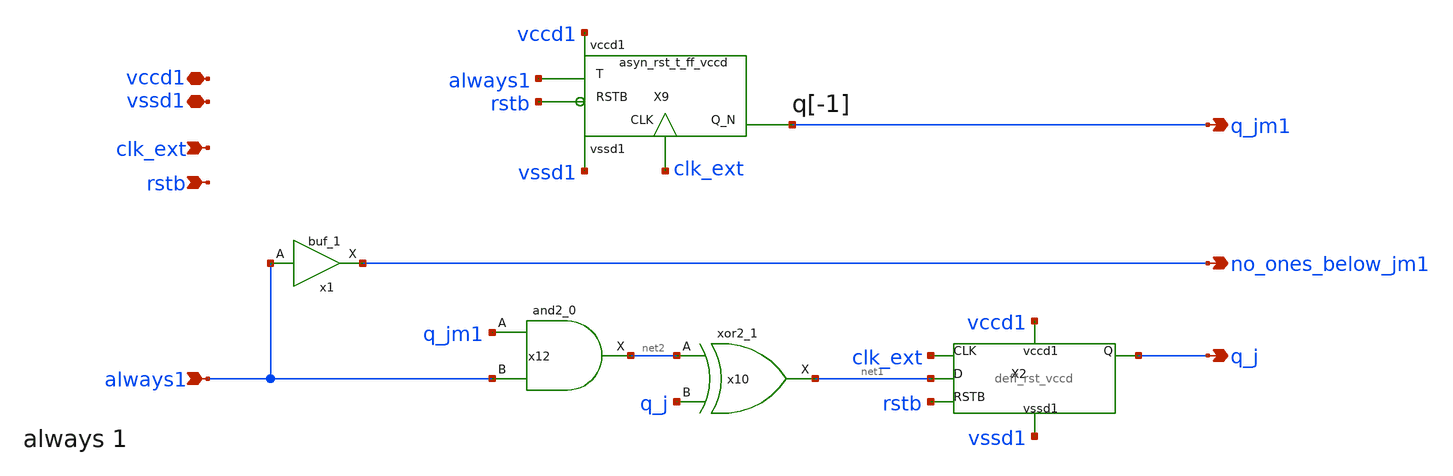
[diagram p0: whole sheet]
** sch_path: xschem/digital/gray_first_cell.sch
**.subckt gray_first_cell vccd1 vssd1 q_j no_ones_below_jm1 clk_ext rstb always1 q_jm1
*.iopin vccd1
*.iopin vssd1
*.opin q_j
*.opin no_ones_below_jm1
*.ipin clk_ext
*.ipin rstb
*.ipin always1
*.opin q_jm1
x10 net2 q_j vssd1 vssd1 vccd1 vccd1 net1 sky130_fd_sc_hd__xor2_1
x12 q_jm1 always1 vssd1 vssd1 vccd1 vccd1 net2 sky130_fd_sc_hd__and2_0
X2 clk_ext net1 q_j rstb vccd1 vssd1 deff_rst_vccd
X9 always1 clk_ext rstb q_jm1 vccd1 vssd1 asyn_rst_t_ff_vccd
x1 always1 vssd1 vssd1 vccd1 vccd1 no_ones_below_jm1 sky130_fd_sc_hd__buf_1
**.ends

* expanding   symbol:  digital/deff_rst_vccd.sym # of pins=6
** sym_path: xschem/digital/deff_rst_vccd.sym
** sch_path: xschem/digital/deff_rst_vccd.sch
.subckt deff_rst_vccd CLK D Q RSTB vccd1 vssd1
*.ipin CLK
*.ipin D
*.opin Q
*.ipin RSTB
*.iopin vccd1
*.iopin vssd1
x3 net1 net2 net3 vssd1 vssd1 vccd1 vccd1 Q sky130_fd_sc_hd__mux2_1
x21 CLK D RSTB vssd1 vssd1 vccd1 vccd1 net1 sky130_fd_sc_hd__dfrtn_1
x1 CLK D RSTB vssd1 vssd1 vccd1 vccd1 net2 sky130_fd_sc_hd__dfrtp_1
x17 net4 vssd1 vssd1 vccd1 vccd1 net5 sky130_fd_sc_hd__buf_1
x2 net5 vssd1 vssd1 vccd1 vccd1 net3 sky130_fd_sc_hd__buf_1
x4 CLK vssd1 vssd1 vccd1 vccd1 net6 sky130_fd_sc_hd__buf_1
x5 net6 vssd1 vssd1 vccd1 vccd1 net4 sky130_fd_sc_hd__buf_1
.ends


* expanding   symbol:  digital/asyn_rst_t_ff_vccd.sym # of pins=6
** sym_path: xschem/digital/asyn_rst_t_ff_vccd.sym
** sch_path: xschem/digital/asyn_rst_t_ff_vccd.sch
.subckt asyn_rst_t_ff_vccd T CLK RSTB Q_N vccd1 vssd1
*.ipin T
*.ipin CLK
*.opin Q_N
*.ipin RSTB
*.iopin vccd1
*.iopin vssd1
x3 T net1 vssd1 vssd1 vccd1 vccd1 net2 sky130_fd_sc_hd__xor2_1
x1 net1 vssd1 vssd1 vccd1 vccd1 Q_N sky130_fd_sc_hd__inv_1
X1 CLK net2 net1 RSTB vccd1 vssd1 deff_rst_vccd
.ends

.end
